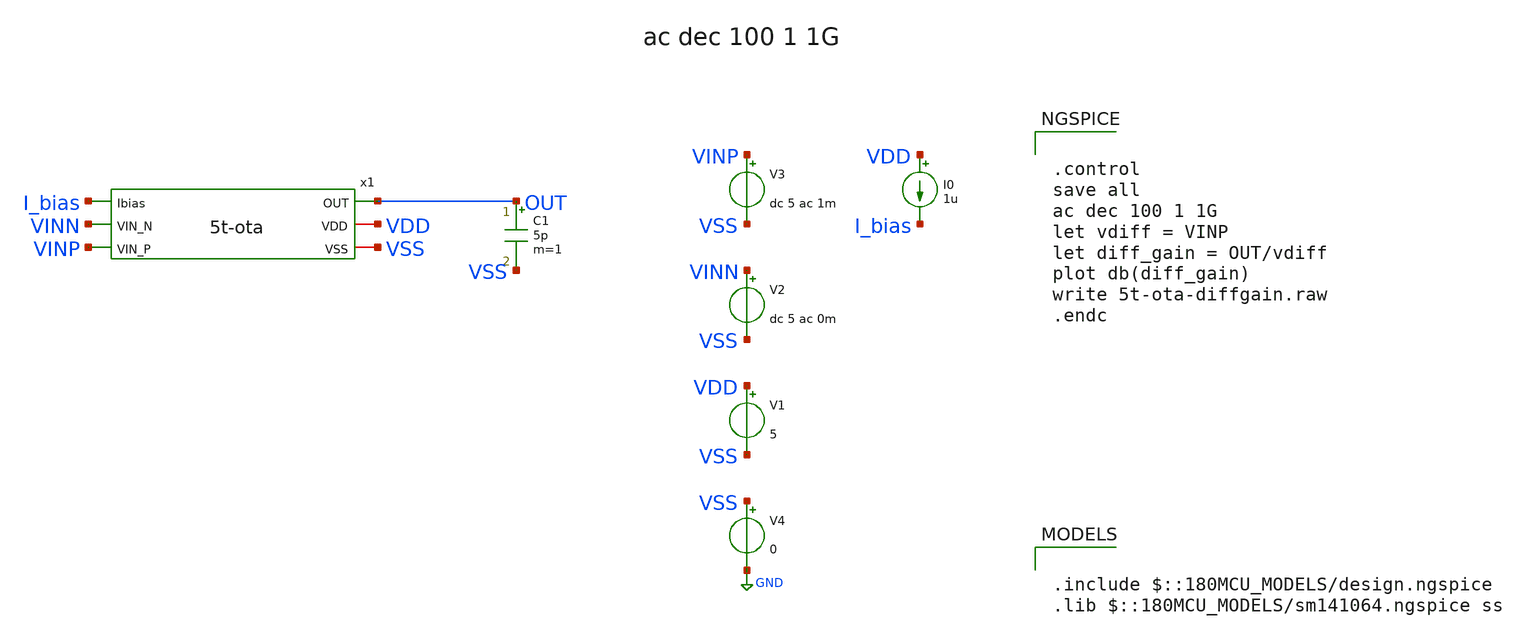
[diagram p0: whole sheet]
** sch_path: week02_current_diffpair/tugas5_cascode_current_mirror/5t-ota-diffgain.sch
**.subckt 5t-ota-diffgain
V1 VDD VSS 5
V2 VINN VSS dc 5 ac 0m
V3 VINP VSS dc 5 ac 1m
V4 VSS GND 0
I0 VDD I_bias 1u
x1 I_bias VINN VINP OUT VDD VSS 5t-ota
C1 OUT VSS 5p m=1
**** begin user architecture code

.include $::180MCU_MODELS/design.ngspice
.lib $::180MCU_MODELS/sm141064.ngspice ss



.control
save all
ac dec 100 1 1G
let vdiff = VINP
let diff_gain = OUT/vdiff
plot db(diff_gain)
write 5t-ota-diffgain.raw
.endc


**** end user architecture code
**.ends

* expanding   symbol:  5t-ota.sym # of pins=6
** sym_path: week02_current_diffpair/tugas5_cascode_current_mirror/5t-ota.sym
** sch_path: week02_current_diffpair/tugas5_cascode_current_mirror/5t-ota.sch
.subckt 5t-ota Ibias VIN_N VIN_P OUT VDD VSS
*.ipin VIN_N
*.ipin VIN_P
*.opin OUT
*.iopin VDD
*.iopin VSS
*.ipin Ibias
XM4 net1 Ibias VSS VSS nfet_06v0 L=1u W=2.5u nf=1 ad='int((nf+1)/2) * W/nf * 0.18u' as='int((nf+2)/2) * W/nf * 0.18u'
+ pd='2*int((nf+1)/2) * (W/nf + 0.18u)' ps='2*int((nf+2)/2) * (W/nf + 0.18u)' nrd='0.18u / W' nrs='0.18u / W'
+ sa=0 sb=0 sd=0 m=1
XM8 Ibias Ibias VSS VSS nfet_06v0 L=1u W=5u nf=1 ad='int((nf+1)/2) * W/nf * 0.18u' as='int((nf+2)/2) * W/nf * 0.18u'
+ pd='2*int((nf+1)/2) * (W/nf + 0.18u)' ps='2*int((nf+2)/2) * (W/nf + 0.18u)' nrd='0.18u / W' nrs='0.18u / W'
+ sa=0 sb=0 sd=0 m=1
XM9 net2 net2 VDD VDD pfet_06v0 L=1u W=5u nf=1 ad='int((nf+1)/2) * W/nf * 0.18u' as='int((nf+2)/2) * W/nf * 0.18u'
+ pd='2*int((nf+1)/2) * (W/nf + 0.18u)' ps='2*int((nf+2)/2) * (W/nf + 0.18u)' nrd='0.18u / W' nrs='0.18u / W'
+ sa=0 sb=0 sd=0 m=1
XM10 OUT VIN_P net1 VSS nfet_06v0 L=1u W=20u nf=1 ad='int((nf+1)/2) * W/nf * 0.18u' as='int((nf+2)/2) * W/nf * 0.18u'
+ pd='2*int((nf+1)/2) * (W/nf + 0.18u)' ps='2*int((nf+2)/2) * (W/nf + 0.18u)' nrd='0.18u / W' nrs='0.18u / W'
+ sa=0 sb=0 sd=0 m=1
XM11 net2 VIN_N net1 VSS nfet_06v0 L=1u W=20u nf=1 ad='int((nf+1)/2) * W/nf * 0.18u' as='int((nf+2)/2) * W/nf * 0.18u'
+ pd='2*int((nf+1)/2) * (W/nf + 0.18u)' ps='2*int((nf+2)/2) * (W/nf + 0.18u)' nrd='0.18u / W' nrs='0.18u / W'
+ sa=0 sb=0 sd=0 m=1
XM12 OUT net2 VDD VDD pfet_06v0 L=1u W=5u nf=1 ad='int((nf+1)/2) * W/nf * 0.18u' as='int((nf+2)/2) * W/nf * 0.18u'
+ pd='2*int((nf+1)/2) * (W/nf + 0.18u)' ps='2*int((nf+2)/2) * (W/nf + 0.18u)' nrd='0.18u / W' nrs='0.18u / W'
+ sa=0 sb=0 sd=0 m=1
.ends

.GLOBAL GND
.end
